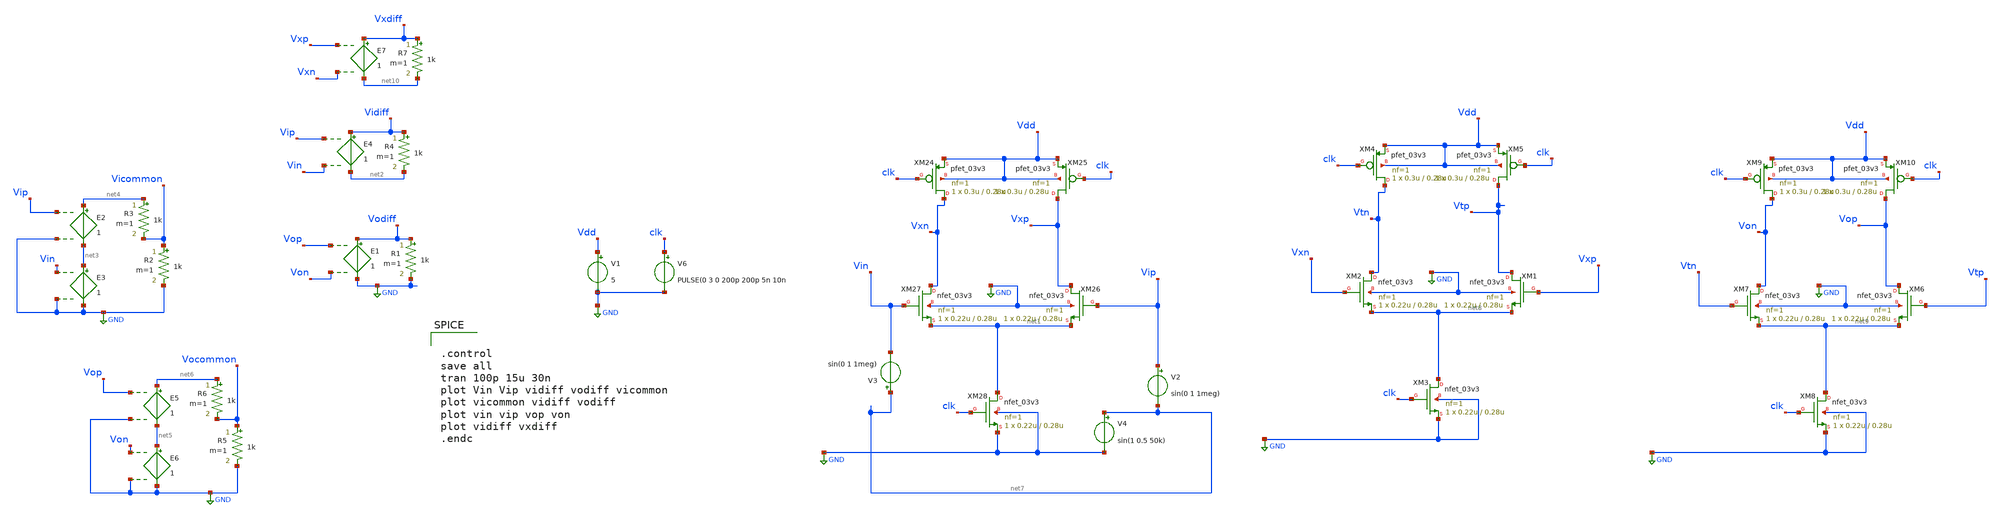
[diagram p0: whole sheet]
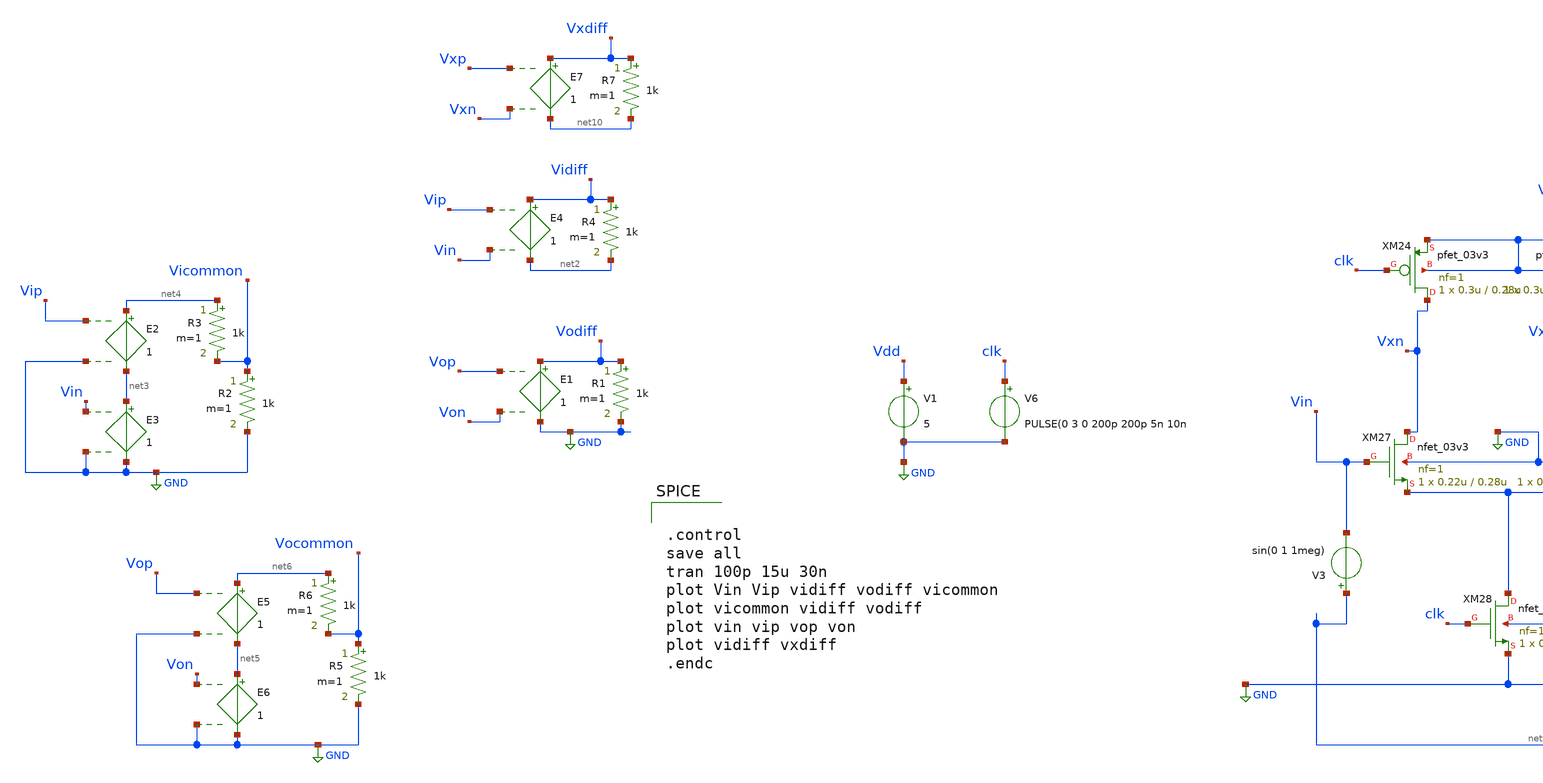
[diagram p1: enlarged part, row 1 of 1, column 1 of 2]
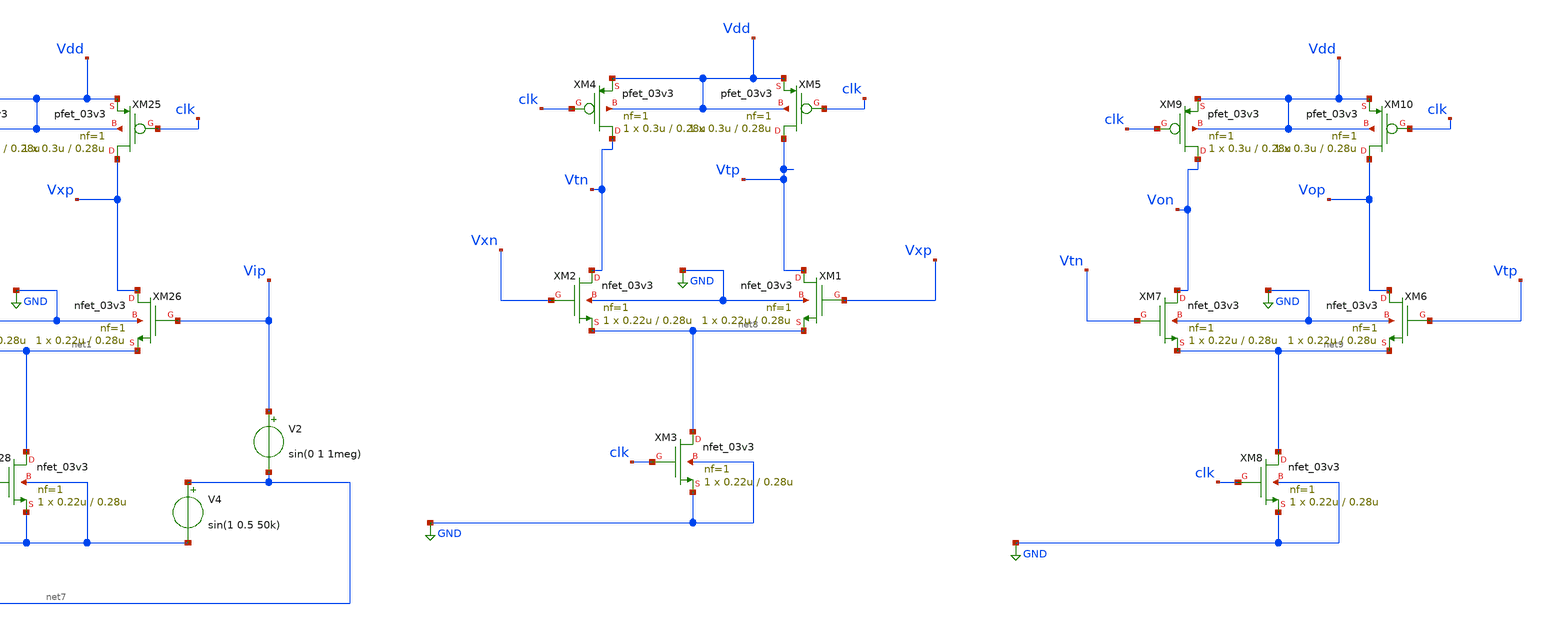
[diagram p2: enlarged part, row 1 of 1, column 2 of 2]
** sch_path: preamp/strongarm_charge_steering_pstage.sch
**.subckt strongarm_charge_steering_pstage
XM26 Vxp Vip net1 GND nfet_03v3 L=0.28u W=0.22u nf=1 ad='int((nf+1)/2) * W/nf * 0.18u' as='int((nf+2)/2) * W/nf * 0.18u'
+ pd='2*int((nf+1)/2) * (W/nf + 0.18u)' ps='2*int((nf+2)/2) * (W/nf + 0.18u)' nrd='0.18u / W' nrs='0.18u / W'
+ sa=0 sb=0 sd=0 m=1
XM27 Vxn Vin net1 GND nfet_03v3 L=0.28u W=0.22u nf=1 ad='int((nf+1)/2) * W/nf * 0.18u' as='int((nf+2)/2) * W/nf * 0.18u'
+ pd='2*int((nf+1)/2) * (W/nf + 0.18u)' ps='2*int((nf+2)/2) * (W/nf + 0.18u)' nrd='0.18u / W' nrs='0.18u / W'
+ sa=0 sb=0 sd=0 m=1
R4 Vidiff net2 1k m=1
E4 Vidiff net2 Vip Vin 1
XM28 net1 clk GND GND nfet_03v3 L=0.28u W=0.22u nf=1 ad='int((nf+1)/2) * W/nf * 0.18u' as='int((nf+2)/2) * W/nf * 0.18u'
+ pd='2*int((nf+1)/2) * (W/nf + 0.18u)' ps='2*int((nf+2)/2) * (W/nf + 0.18u)' nrd='0.18u / W' nrs='0.18u / W'
+ sa=0 sb=0 sd=0 m=1
XM24 Vxn clk Vdd Vdd pfet_03v3 L=0.28u W=0.3u nf=1 ad='int((nf+1)/2) * W/nf * 0.18u' as='int((nf+2)/2) * W/nf * 0.18u'
+ pd='2*int((nf+1)/2) * (W/nf + 0.18u)' ps='2*int((nf+2)/2) * (W/nf + 0.18u)' nrd='0.18u / W' nrs='0.18u / W'
+ sa=0 sb=0 sd=0 m=1
XM25 Vxp clk Vdd Vdd pfet_03v3 L=0.28u W=0.3u nf=1 ad='int((nf+1)/2) * W/nf * 0.18u' as='int((nf+2)/2) * W/nf * 0.18u'
+ pd='2*int((nf+1)/2) * (W/nf + 0.18u)' ps='2*int((nf+2)/2) * (W/nf + 0.18u)' nrd='0.18u / W' nrs='0.18u / W'
+ sa=0 sb=0 sd=0 m=1
R1 Vodiff GND 1k m=1
E1 Vodiff GND Vop Von 1
V6 clk GND PULSE(0 3 0 200p 200p 5n 10n
V2 Vip net7 sin(0 1 1meg)
E2 net4 net3 Vip GND 1
E3 net3 GND Vin GND 1
R2 Vicommon GND 1k m=1
R3 net4 Vicommon 1k m=1
E5 net6 net5 Vop GND 1
E6 net5 GND Von GND 1
R5 Vocommon GND 1k m=1
R6 net6 Vocommon 1k m=1
V1 Vdd GND 5
V4 net7 GND sin(1 0.5 50k)
V3 net7 Vin sin(0 1 1meg)
XM1 Vtp Vxp net8 GND nfet_03v3 L=0.28u W=0.22u nf=1 ad='int((nf+1)/2) * W/nf * 0.18u' as='int((nf+2)/2) * W/nf * 0.18u'
+ pd='2*int((nf+1)/2) * (W/nf + 0.18u)' ps='2*int((nf+2)/2) * (W/nf + 0.18u)' nrd='0.18u / W' nrs='0.18u / W'
+ sa=0 sb=0 sd=0 m=1
XM2 Vtn Vxn net8 GND nfet_03v3 L=0.28u W=0.22u nf=1 ad='int((nf+1)/2) * W/nf * 0.18u' as='int((nf+2)/2) * W/nf * 0.18u'
+ pd='2*int((nf+1)/2) * (W/nf + 0.18u)' ps='2*int((nf+2)/2) * (W/nf + 0.18u)' nrd='0.18u / W' nrs='0.18u / W'
+ sa=0 sb=0 sd=0 m=1
XM3 net8 clk GND GND nfet_03v3 L=0.28u W=0.22u nf=1 ad='int((nf+1)/2) * W/nf * 0.18u' as='int((nf+2)/2) * W/nf * 0.18u'
+ pd='2*int((nf+1)/2) * (W/nf + 0.18u)' ps='2*int((nf+2)/2) * (W/nf + 0.18u)' nrd='0.18u / W' nrs='0.18u / W'
+ sa=0 sb=0 sd=0 m=1
XM4 Vtn clk Vdd Vdd pfet_03v3 L=0.28u W=0.3u nf=1 ad='int((nf+1)/2) * W/nf * 0.18u' as='int((nf+2)/2) * W/nf * 0.18u'
+ pd='2*int((nf+1)/2) * (W/nf + 0.18u)' ps='2*int((nf+2)/2) * (W/nf + 0.18u)' nrd='0.18u / W' nrs='0.18u / W'
+ sa=0 sb=0 sd=0 m=1
XM5 Vtp clk Vdd Vdd pfet_03v3 L=0.28u W=0.3u nf=1 ad='int((nf+1)/2) * W/nf * 0.18u' as='int((nf+2)/2) * W/nf * 0.18u'
+ pd='2*int((nf+1)/2) * (W/nf + 0.18u)' ps='2*int((nf+2)/2) * (W/nf + 0.18u)' nrd='0.18u / W' nrs='0.18u / W'
+ sa=0 sb=0 sd=0 m=1
XM6 Vop Vtp net9 GND nfet_03v3 L=0.28u W=0.22u nf=1 ad='int((nf+1)/2) * W/nf * 0.18u' as='int((nf+2)/2) * W/nf * 0.18u'
+ pd='2*int((nf+1)/2) * (W/nf + 0.18u)' ps='2*int((nf+2)/2) * (W/nf + 0.18u)' nrd='0.18u / W' nrs='0.18u / W'
+ sa=0 sb=0 sd=0 m=1
XM7 Von Vtn net9 GND nfet_03v3 L=0.28u W=0.22u nf=1 ad='int((nf+1)/2) * W/nf * 0.18u' as='int((nf+2)/2) * W/nf * 0.18u'
+ pd='2*int((nf+1)/2) * (W/nf + 0.18u)' ps='2*int((nf+2)/2) * (W/nf + 0.18u)' nrd='0.18u / W' nrs='0.18u / W'
+ sa=0 sb=0 sd=0 m=1
XM8 net9 clk GND GND nfet_03v3 L=0.28u W=0.22u nf=1 ad='int((nf+1)/2) * W/nf * 0.18u' as='int((nf+2)/2) * W/nf * 0.18u'
+ pd='2*int((nf+1)/2) * (W/nf + 0.18u)' ps='2*int((nf+2)/2) * (W/nf + 0.18u)' nrd='0.18u / W' nrs='0.18u / W'
+ sa=0 sb=0 sd=0 m=1
XM9 Von clk Vdd Vdd pfet_03v3 L=0.28u W=0.3u nf=1 ad='int((nf+1)/2) * W/nf * 0.18u' as='int((nf+2)/2) * W/nf * 0.18u'
+ pd='2*int((nf+1)/2) * (W/nf + 0.18u)' ps='2*int((nf+2)/2) * (W/nf + 0.18u)' nrd='0.18u / W' nrs='0.18u / W'
+ sa=0 sb=0 sd=0 m=1
XM10 Vop clk Vdd Vdd pfet_03v3 L=0.28u W=0.3u nf=1 ad='int((nf+1)/2) * W/nf * 0.18u' as='int((nf+2)/2) * W/nf * 0.18u'
+ pd='2*int((nf+1)/2) * (W/nf + 0.18u)' ps='2*int((nf+2)/2) * (W/nf + 0.18u)' nrd='0.18u / W' nrs='0.18u / W'
+ sa=0 sb=0 sd=0 m=1
R7 Vxdiff net10 1k m=1
E7 Vxdiff net10 Vxp Vxn 1
**** begin user architecture code

.include /foss/pdks/gf180mcuC/libs.tech/ngspice/design.ngspice
.lib /foss/pdks/gf180mcuC/libs.tech/ngspice/sm141064.ngspice typical



.control
save all
tran 100p 15u 30n
plot Vin Vip vidiff vodiff vicommon
plot vicommon vidiff vodiff
plot vin vip vop von
plot vidiff vxdiff
.endc

**** end user architecture code
**.ends
.GLOBAL GND
.end
